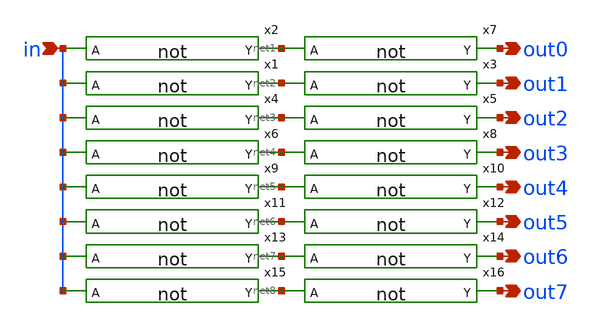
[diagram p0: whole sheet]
** sch_path: elements/buf8.sch
**.subckt buf8 in out0 out1 out2 out3 out4 out5 out6 out7
*.ipin in
*.opin out0
*.opin out1
*.opin out2
*.opin out3
*.opin out4
*.opin out5
*.opin out6
*.opin out7
x2 in net1 not
x7 net1 out0 not
x1 in net2 not
x3 net2 out1 not
x4 in net3 not
x5 net3 out2 not
x6 in net4 not
x8 net4 out3 not
x9 in net5 not
x10 net5 out4 not
x11 in net6 not
x12 net6 out5 not
x13 in net7 not
x14 net7 out6 not
x15 in net8 not
x16 net8 out7 not
**.ends

* expanding   symbol:  /home/andreil/ASIC/elements/not.sym # of pins=2
** sym_path: elements/not.sym
** sch_path: elements/not.sch
.subckt not A Y
*.ipin A
*.opin Y
XM1 Y A VCC VCC sky130_fd_pr__pfet_01v8 L=0.15 W=1 nf=1 ad='int((nf+1)/2) * W/nf * 0.29' as='int((nf+2)/2) * W/nf * 0.29'
+ pd='2*int((nf+1)/2) * (W/nf + 0.29)' ps='2*int((nf+2)/2) * (W/nf + 0.29)' nrd='0.29 / W' nrs='0.29 / W'
+ sa=0 sb=0 sd=0 mult=1 m=1
XM2 Y A VSS VSS sky130_fd_pr__nfet_01v8 L=0.15 W=0.65 nf=1 ad='int((1 + 1)/2) * 0.65 / 1 * 0.29' as='int((1 + 2)/2) * 0.65 / 1 * 0.29'
+ pd='2*int((1 + 1)/2) * (0.65 / 1 + 0.29)' ps='2*int((1 + 2)/2) * (0.65 / 1 + 0.29)' nrd='0.29 / 0.65 '
+ nrs='0.29 / 0.65 ' sa=0 sb=0 sd=0 mult=1 m=1
.ends

.GLOBAL VCC
.GLOBAL VSS
.end
